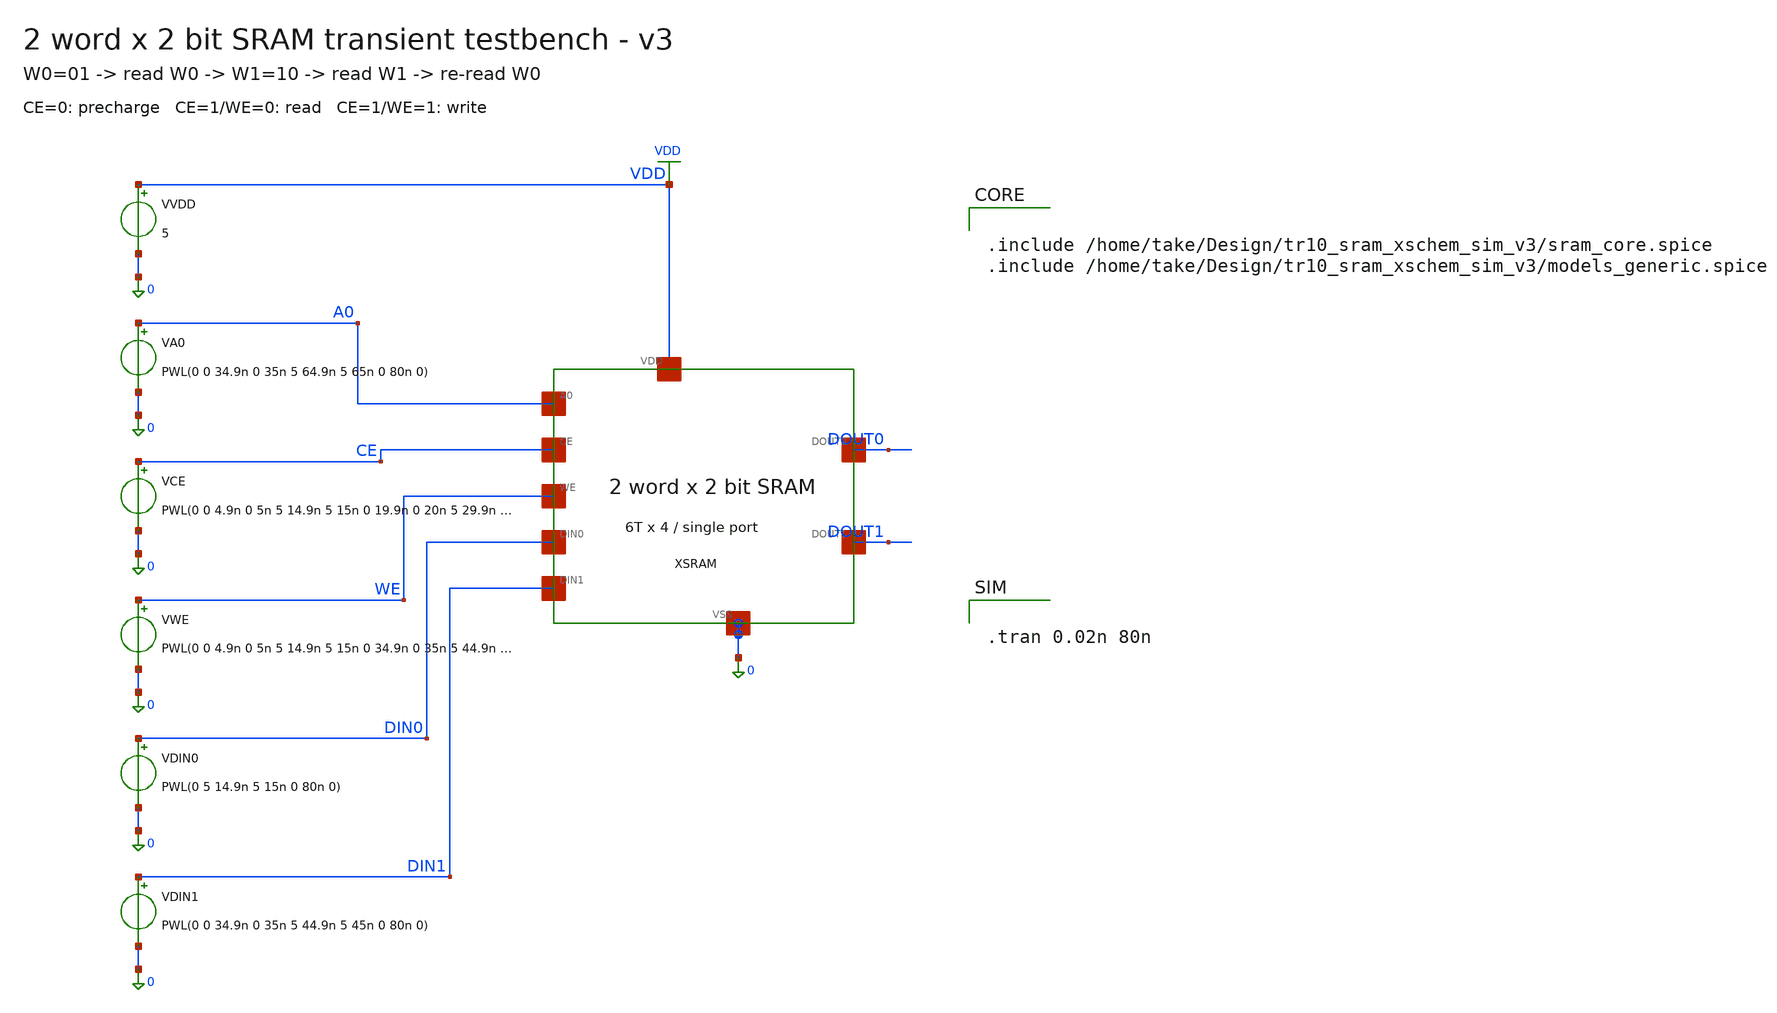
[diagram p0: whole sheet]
** sch_path: generic/tr10_sram_xschem_sim_v3/tb_sram_2x2.sch
**.subckt tb_sram_2x2
XXSRAM A0 CE WE DIN0 DIN1 DOUT0 DOUT1 net1 0 SRAM2X2
VVDD VDD 0 5
VA0 A0 0 PWL(0 0 34.9n 0 35n 5 64.9n 5 65n 0 80n 0)
VCE CE 0 PWL(0 0 4.9n 0 5n 5 14.9n 5 15n 0 19.9n 0 20n 5 29.9n 5 30n 0 34.9n 0 35n 5 44.9n 5 45n 0
+ 49.9n 0 50n 5 59.9n 5 60n 0 64.9n 0 65n 5 74.9n 5 75n 0 80n 0)
VWE WE 0 PWL(0 0 4.9n 0 5n 5 14.9n 5 15n 0 34.9n 0 35n 5 44.9n 5 45n 0 80n 0)
VDIN0 DIN0 0 PWL(0 5 14.9n 5 15n 0 80n 0)
VDIN1 DIN1 0 PWL(0 0 34.9n 0 35n 5 44.9n 5 45n 0 80n 0)
**** begin user architecture code


.include /home/take/Design/tr10_sram_xschem_sim_v3/sram_core.spice
.include /home/take/Design/tr10_sram_xschem_sim_v3/models_generic.spice




.tran 0.02n 80n


**** end user architecture code
**.ends
.GLOBAL VDD
.end
